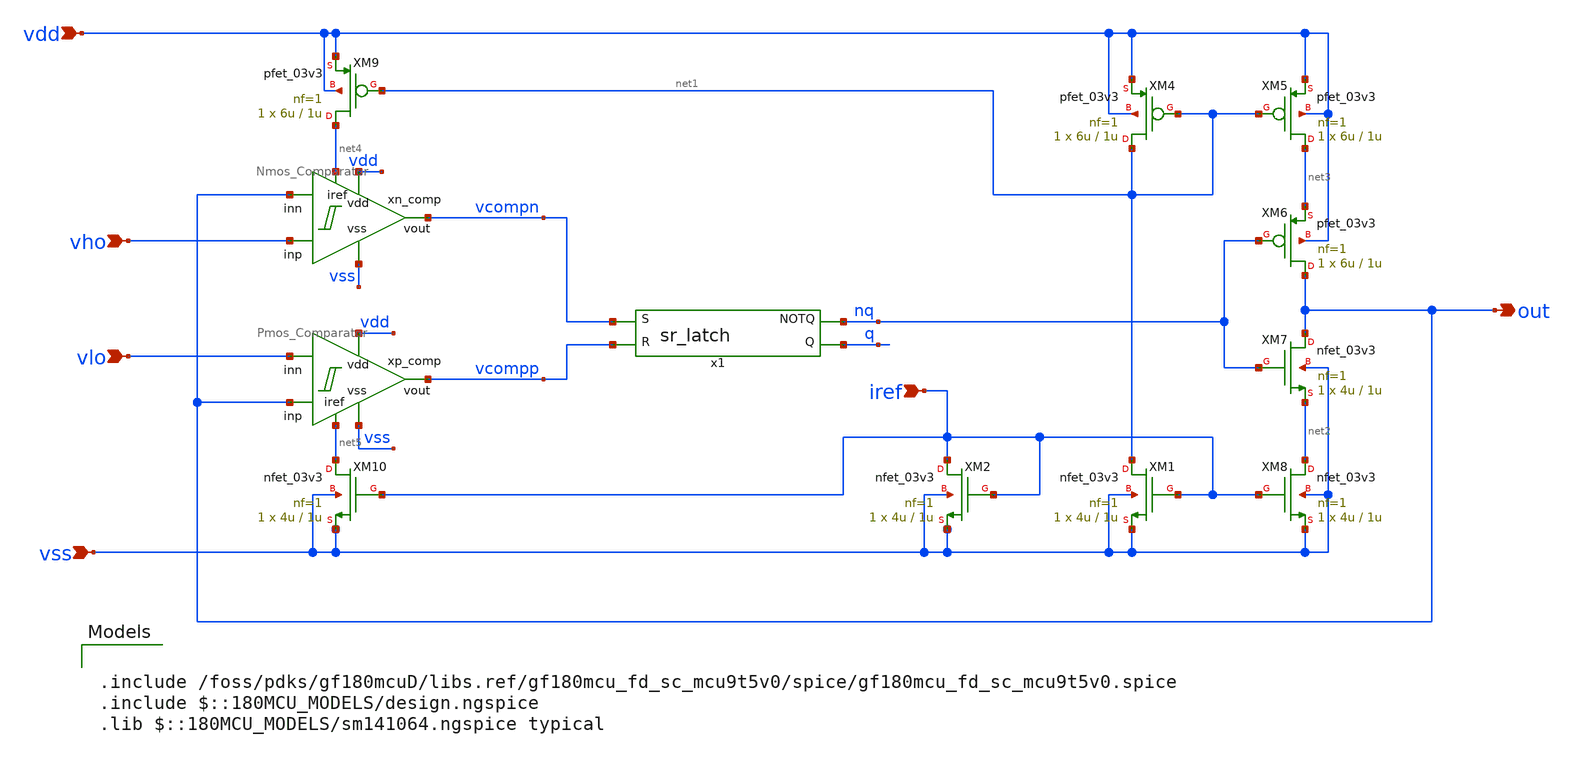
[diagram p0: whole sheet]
** sch_path: designs/libs/core_analog/oscillator/triangle_osc.sch
**.subckt triangle_osc iref vss vho vlo out vdd
*.ipin iref
*.ipin vss
*.ipin vho
*.ipin vlo
*.opin out
*.ipin vdd
XM1 net1 iref vss vss nfet_03v3 L=1u W=4u nf=1 ad='int((nf+1)/2) * W/nf * 0.18u' as='int((nf+2)/2) * W/nf * 0.18u'
+ pd='2*int((nf+1)/2) * (W/nf + 0.18u)' ps='2*int((nf+2)/2) * (W/nf + 0.18u)' nrd='0.18u / W' nrs='0.18u / W'
+ sa=0 sb=0 sd=0 m=1
XM8 net2 iref vss vss nfet_03v3 L=1u W=4u nf=1 ad='int((nf+1)/2) * W/nf * 0.18u' as='int((nf+2)/2) * W/nf * 0.18u'
+ pd='2*int((nf+1)/2) * (W/nf + 0.18u)' ps='2*int((nf+2)/2) * (W/nf + 0.18u)' nrd='0.18u / W' nrs='0.18u / W'
+ sa=0 sb=0 sd=0 m=1
XM4 net1 net1 vdd vdd pfet_03v3 L=1u W=6u nf=1 ad='int((nf+1)/2) * W/nf * 0.18u' as='int((nf+2)/2) * W/nf * 0.18u'
+ pd='2*int((nf+1)/2) * (W/nf + 0.18u)' ps='2*int((nf+2)/2) * (W/nf + 0.18u)' nrd='0.18u / W' nrs='0.18u / W'
+ sa=0 sb=0 sd=0 m=1
XM5 net3 net1 vdd vdd pfet_03v3 L=1u W=6u nf=1 ad='int((nf+1)/2) * W/nf * 0.18u' as='int((nf+2)/2) * W/nf * 0.18u'
+ pd='2*int((nf+1)/2) * (W/nf + 0.18u)' ps='2*int((nf+2)/2) * (W/nf + 0.18u)' nrd='0.18u / W' nrs='0.18u / W'
+ sa=0 sb=0 sd=0 m=1
XM6 out nq net3 vdd pfet_03v3 L=1u W=6u nf=1 ad='int((nf+1)/2) * W/nf * 0.18u' as='int((nf+2)/2) * W/nf * 0.18u'
+ pd='2*int((nf+1)/2) * (W/nf + 0.18u)' ps='2*int((nf+2)/2) * (W/nf + 0.18u)' nrd='0.18u / W' nrs='0.18u / W'
+ sa=0 sb=0 sd=0 m=1
XM7 out nq net2 vss nfet_03v3 L=1u W=4u nf=1 ad='int((nf+1)/2) * W/nf * 0.18u' as='int((nf+2)/2) * W/nf * 0.18u'
+ pd='2*int((nf+1)/2) * (W/nf + 0.18u)' ps='2*int((nf+2)/2) * (W/nf + 0.18u)' nrd='0.18u / W' nrs='0.18u / W'
+ sa=0 sb=0 sd=0 m=1
XM2 iref iref vss vss nfet_03v3 L=1u W=4u nf=1 ad='int((nf+1)/2) * W/nf * 0.18u' as='int((nf+2)/2) * W/nf * 0.18u'
+ pd='2*int((nf+1)/2) * (W/nf + 0.18u)' ps='2*int((nf+2)/2) * (W/nf + 0.18u)' nrd='0.18u / W' nrs='0.18u / W'
+ sa=0 sb=0 sd=0 m=1
XM10 net5 iref vss vss nfet_03v3 L=1u W=4u nf=1 ad='int((nf+1)/2) * W/nf * 0.18u' as='int((nf+2)/2) * W/nf * 0.18u'
+ pd='2*int((nf+1)/2) * (W/nf + 0.18u)' ps='2*int((nf+2)/2) * (W/nf + 0.18u)' nrd='0.18u / W' nrs='0.18u / W'
+ sa=0 sb=0 sd=0 m=1
XM9 net4 net1 vdd vdd pfet_03v3 L=1u W=6u nf=1 ad='int((nf+1)/2) * W/nf * 0.18u' as='int((nf+2)/2) * W/nf * 0.18u'
+ pd='2*int((nf+1)/2) * (W/nf + 0.18u)' ps='2*int((nf+2)/2) * (W/nf + 0.18u)' nrd='0.18u / W' nrs='0.18u / W'
+ sa=0 sb=0 sd=0 m=1
xn_comp vdd vcompn vho vss out net4 Nmos_Comparator
xp_comp vdd vcompp out vss vlo net5 Pmos_Comparator
x1 vcompp q nq vcompn sr_latch
**** begin user architecture code

.include /foss/pdks/gf180mcuD/libs.ref/gf180mcu_fd_sc_mcu9t5v0/spice/gf180mcu_fd_sc_mcu9t5v0.spice
.include $::180MCU_MODELS/design.ngspice
.lib $::180MCU_MODELS/sm141064.ngspice typical

**** end user architecture code
**.ends

* expanding   symbol:  libs/core_analog/Comparator/Nmos_Comparator.sym # of pins=6
** sym_path: designs/libs/core_analog/Comparator/Nmos_Comparator.sym
** sch_path: designs/libs/core_analog/Comparator/Nmos_Comparator.sch
.subckt Nmos_Comparator vdd vout inp vss inn iref
*.ipin vss
*.ipin vdd
*.ipin iref
*.ipin inn
*.ipin inp
*.opin vout
XM3 v_3_7_n v_3_7_n vss vss nfet_03v3 L=1u W=3.5u nf=1 ad='int((nf+1)/2) * W/nf * 0.18u' as='int((nf+2)/2) * W/nf * 0.18u'
+ pd='2*int((nf+1)/2) * (W/nf + 0.18u)' ps='2*int((nf+2)/2) * (W/nf + 0.18u)' nrd='0.18u / W' nrs='0.18u / W'
+ sa=0 sb=0 sd=0 m=1
XM4 vout v_3_7_n vss vss nfet_03v3 L=1u W=3.5u nf=1 ad='int((nf+1)/2) * W/nf * 0.18u' as='int((nf+2)/2) * W/nf * 0.18u'
+ pd='2*int((nf+1)/2) * (W/nf + 0.18u)' ps='2*int((nf+2)/2) * (W/nf + 0.18u)' nrd='0.18u / W' nrs='0.18u / W'
+ sa=0 sb=0 sd=0 m=1
XM5 v_5_11_n inn i_bias_n vss nfet_03v3 L=1u W=4u nf=1 ad='int((nf+1)/2) * W/nf * 0.18u' as='int((nf+2)/2) * W/nf * 0.18u'
+ pd='2*int((nf+1)/2) * (W/nf + 0.18u)' ps='2*int((nf+2)/2) * (W/nf + 0.18u)' nrd='0.18u / W' nrs='0.18u / W'
+ sa=0 sb=0 sd=0 m=1
XM6 v_6_9_n inp i_bias_n vss nfet_03v3 L=1u W=4u nf=1 ad='int((nf+1)/2) * W/nf * 0.18u' as='int((nf+2)/2) * W/nf * 0.18u'
+ pd='2*int((nf+1)/2) * (W/nf + 0.18u)' ps='2*int((nf+2)/2) * (W/nf + 0.18u)' nrd='0.18u / W' nrs='0.18u / W'
+ sa=0 sb=0 sd=0 m=1
XM7 v_3_7_n v_5_11_n vdd vdd pfet_03v3 L=0.5u W=16.5u nf=4 ad='int((nf+1)/2) * W/nf * 0.18u' as='int((nf+2)/2) * W/nf * 0.18u'
+ pd='2*int((nf+1)/2) * (W/nf + 0.18u)' ps='2*int((nf+2)/2) * (W/nf + 0.18u)' nrd='0.18u / W' nrs='0.18u / W'
+ sa=0 sb=0 sd=0 m=1
XM9 v_6_9_n v_6_9_n vdd vdd pfet_03v3 L=0.5u W=10u nf=2 ad='int((nf+1)/2) * W/nf * 0.18u' as='int((nf+2)/2) * W/nf * 0.18u'
+ pd='2*int((nf+1)/2) * (W/nf + 0.18u)' ps='2*int((nf+2)/2) * (W/nf + 0.18u)' nrd='0.18u / W' nrs='0.18u / W'
+ sa=0 sb=0 sd=0 m=1
XM11 v_5_11_n v_5_11_n vdd vdd pfet_03v3 L=0.5u W=10u nf=2 ad='int((nf+1)/2) * W/nf * 0.18u' as='int((nf+2)/2) * W/nf * 0.18u'
+ pd='2*int((nf+1)/2) * (W/nf + 0.18u)' ps='2*int((nf+2)/2) * (W/nf + 0.18u)' nrd='0.18u / W' nrs='0.18u / W'
+ sa=0 sb=0 sd=0 m=1
XM12 vout v_6_9_n vdd vdd pfet_03v3 L=0.5u W=16.5u nf=4 ad='int((nf+1)/2) * W/nf * 0.18u' as='int((nf+2)/2) * W/nf * 0.18u'
+ pd='2*int((nf+1)/2) * (W/nf + 0.18u)' ps='2*int((nf+2)/2) * (W/nf + 0.18u)' nrd='0.18u / W' nrs='0.18u / W'
+ sa=0 sb=0 sd=0 m=1
XM1 v_6_9_n v_5_11_n vdd vdd pfet_03v3 L=0.5u W=10u nf=2 ad='int((nf+1)/2) * W/nf * 0.18u' as='int((nf+2)/2) * W/nf * 0.18u'
+ pd='2*int((nf+1)/2) * (W/nf + 0.18u)' ps='2*int((nf+2)/2) * (W/nf + 0.18u)' nrd='0.18u / W' nrs='0.18u / W'
+ sa=0 sb=0 sd=0 m=1
XM2 v_5_11_n v_6_9_n vdd vdd pfet_03v3 L=0.5u W=10u nf=2 ad='int((nf+1)/2) * W/nf * 0.18u' as='int((nf+2)/2) * W/nf * 0.18u'
+ pd='2*int((nf+1)/2) * (W/nf + 0.18u)' ps='2*int((nf+2)/2) * (W/nf + 0.18u)' nrd='0.18u / W' nrs='0.18u / W'
+ sa=0 sb=0 sd=0 m=1
XM8 iref iref vss vss nfet_03v3 L=1u W=2.5u nf=1 ad='int((nf+1)/2) * W/nf * 0.18u' as='int((nf+2)/2) * W/nf * 0.18u'
+ pd='2*int((nf+1)/2) * (W/nf + 0.18u)' ps='2*int((nf+2)/2) * (W/nf + 0.18u)' nrd='0.18u / W' nrs='0.18u / W'
+ sa=0 sb=0 sd=0 m=1
XM10 i_bias_n iref vss vss nfet_03v3 L=1u W=5u nf=2 ad='int((nf+1)/2) * W/nf * 0.18u' as='int((nf+2)/2) * W/nf * 0.18u'
+ pd='2*int((nf+1)/2) * (W/nf + 0.18u)' ps='2*int((nf+2)/2) * (W/nf + 0.18u)' nrd='0.18u / W' nrs='0.18u / W'
+ sa=0 sb=0 sd=0 m=1
.ends


* expanding   symbol:  libs/core_analog/oscillator/sr_latch.sym # of pins=4
** sym_path: designs/libs/core_analog/oscillator/sr_latch.sym
** sch_path: designs/libs/core_analog/oscillator/sr_latch.sch
.subckt sr_latch R Q NOTQ S
*.ipin R
*.ipin S
*.opin Q
*.opin NOTQ
x1 R NOTQ VSSd VDDd VSSd VDDd Q gf180mcu_fd_sc_mcu9t5v0__nor2_2
x2 Q S VSSd VDDd VSSd VDDd NOTQ gf180mcu_fd_sc_mcu9t5v0__nor2_2
**** begin user architecture code

.include $::180MCU_MODELS/design.ngspice
.include /foss/pdks/gf180mcuD/libs.ref/gf180mcu_fd_sc_mcu9t5v0/spice/gf180mcu_fd_sc_mcu9t5v0.spice
.lib $::180MCU_MODELS/sm141064.ngspice typical

**** end user architecture code
.ends

.end
